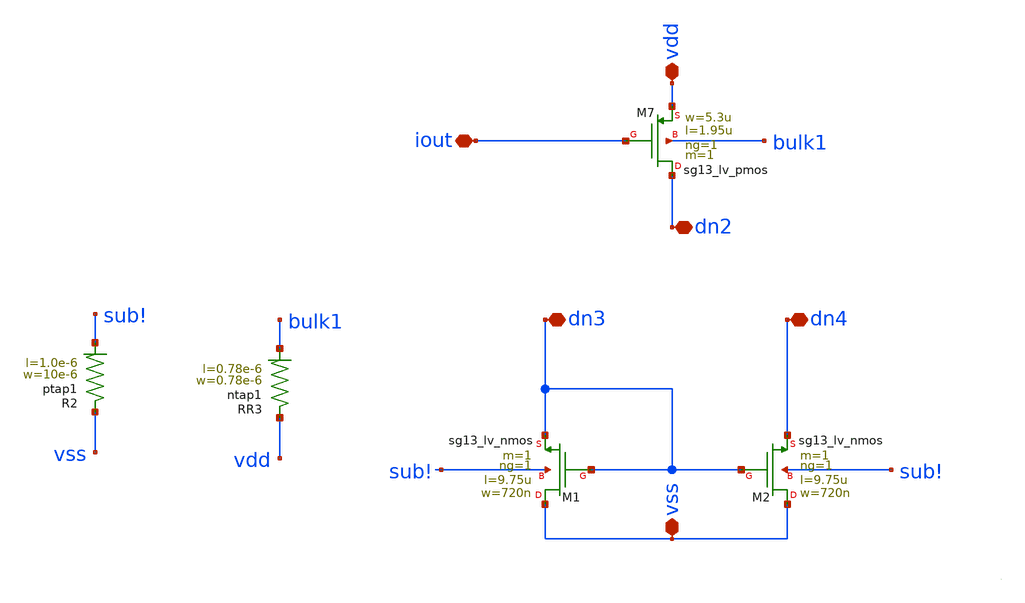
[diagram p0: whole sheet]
** sch_path: schematic/bgr/part_3_layout/OTA_layout/input_stage/schematic_mod/input_stage.sch
**.subckt input_stage vss vdd dn4 dn3 dn2 iout
*.iopin vss
*.iopin vdd
*.iopin dn4
*.iopin dn3
*.iopin dn2
*.iopin iout
XM7 dn2 iout vdd bulk1 sg13_lv_pmos w=5.3u l=1.95u ng=1 m=1 mm_ok=1
XR2 vss sub! ptap1 R=30.62 w=10e-6 l=1.0e-6
XR3 vdd bulk1 ntap1 R=262.8 w=0.78e-6 l=0.78e-6
XM1 vss dn3 dn3 sub! sg13_lv_nmos w=720n l=9.75u ng=1 m=1 mm_ok=1
XM2 vss dn3 dn4 sub! sg13_lv_nmos w=720n l=9.75u ng=1 m=1 mm_ok=1
**.ends
.end
